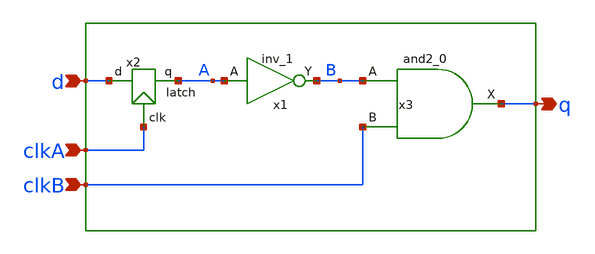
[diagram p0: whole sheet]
** sch_path: src/xe/test_cases/latch_and.sch
**.subckt latch_and d clkA q clkB
*.ipin d
*.ipin clkA
*.opin q
*.ipin clkB
x1 A vcc vcc vss vss B sky130_fd_sc_hd__inv_1
x3 B clkB vss vss vcc vcc q sky130_fd_sc_hd__and2_0
x2 clkA A d latch
**.ends

* expanding   symbol:  yxt/latch.sym # of pins=3
** sym_path: src/xe/test_cases/latch.sym
** sch_path: src/xe/test_cases/latch.sch
.subckt latch clk q d  vcc=vcc vss=vss
*.ipin clk
*.ipin d
*.opin q
x1 d vcc vcc vss vss db sky130_fd_sc_hd__inv_1
x2 clkb db z clk tgate vcc=vcc vss=vss
x3 z vcc vcc vss vss q sky130_fd_sc_hd__inv_1
x6 clk vcc vcc vss vss clkb sky130_fd_sc_hd__inv_1
x4 z vcc vcc vss vss fb sky130_fd_sc_hd__inv_1
x5 fb vcc vcc vss vss z sky130_fd_sc_hd__inv_1
.ends


* expanding   symbol:  yxt/tgate.sym # of pins=4
** sym_path: src/xe/test_cases/tgate.sym
** sch_path: src/xe/test_cases/tgate.sch
.subckt tgate gp s d gn  vcc=vcc vss=vss
*.ipin s
*.ipin gp
*.ipin gn
*.opin d
XMpc d gp s vss sky130_fd_pr__pfet_01v8 L=0.15 W=1 nf=1 ad='int((nf+1)/2) * W/nf * 0.29' as='int((nf+2)/2) * W/nf * 0.29'
+ pd='2*int((nf+1)/2) * (W/nf + 0.29)' ps='2*int((nf+2)/2) * (W/nf + 0.29)' nrd='0.29 / W' nrs='0.29 / W'
+ sa=0 sb=0 sd=0 mult=7 m=7
XM15 s gn d vcc sky130_fd_pr__nfet_01v8 L=0.15 W=1 nf=1 ad='int((nf+1)/2) * W/nf * 0.29' as='int((nf+2)/2) * W/nf * 0.29'
+ pd='2*int((nf+1)/2) * (W/nf + 0.29)' ps='2*int((nf+2)/2) * (W/nf + 0.29)' nrd='0.29 / W' nrs='0.29 / W'
+ sa=0 sb=0 sd=0 mult=1 m=1
.ends

.end
